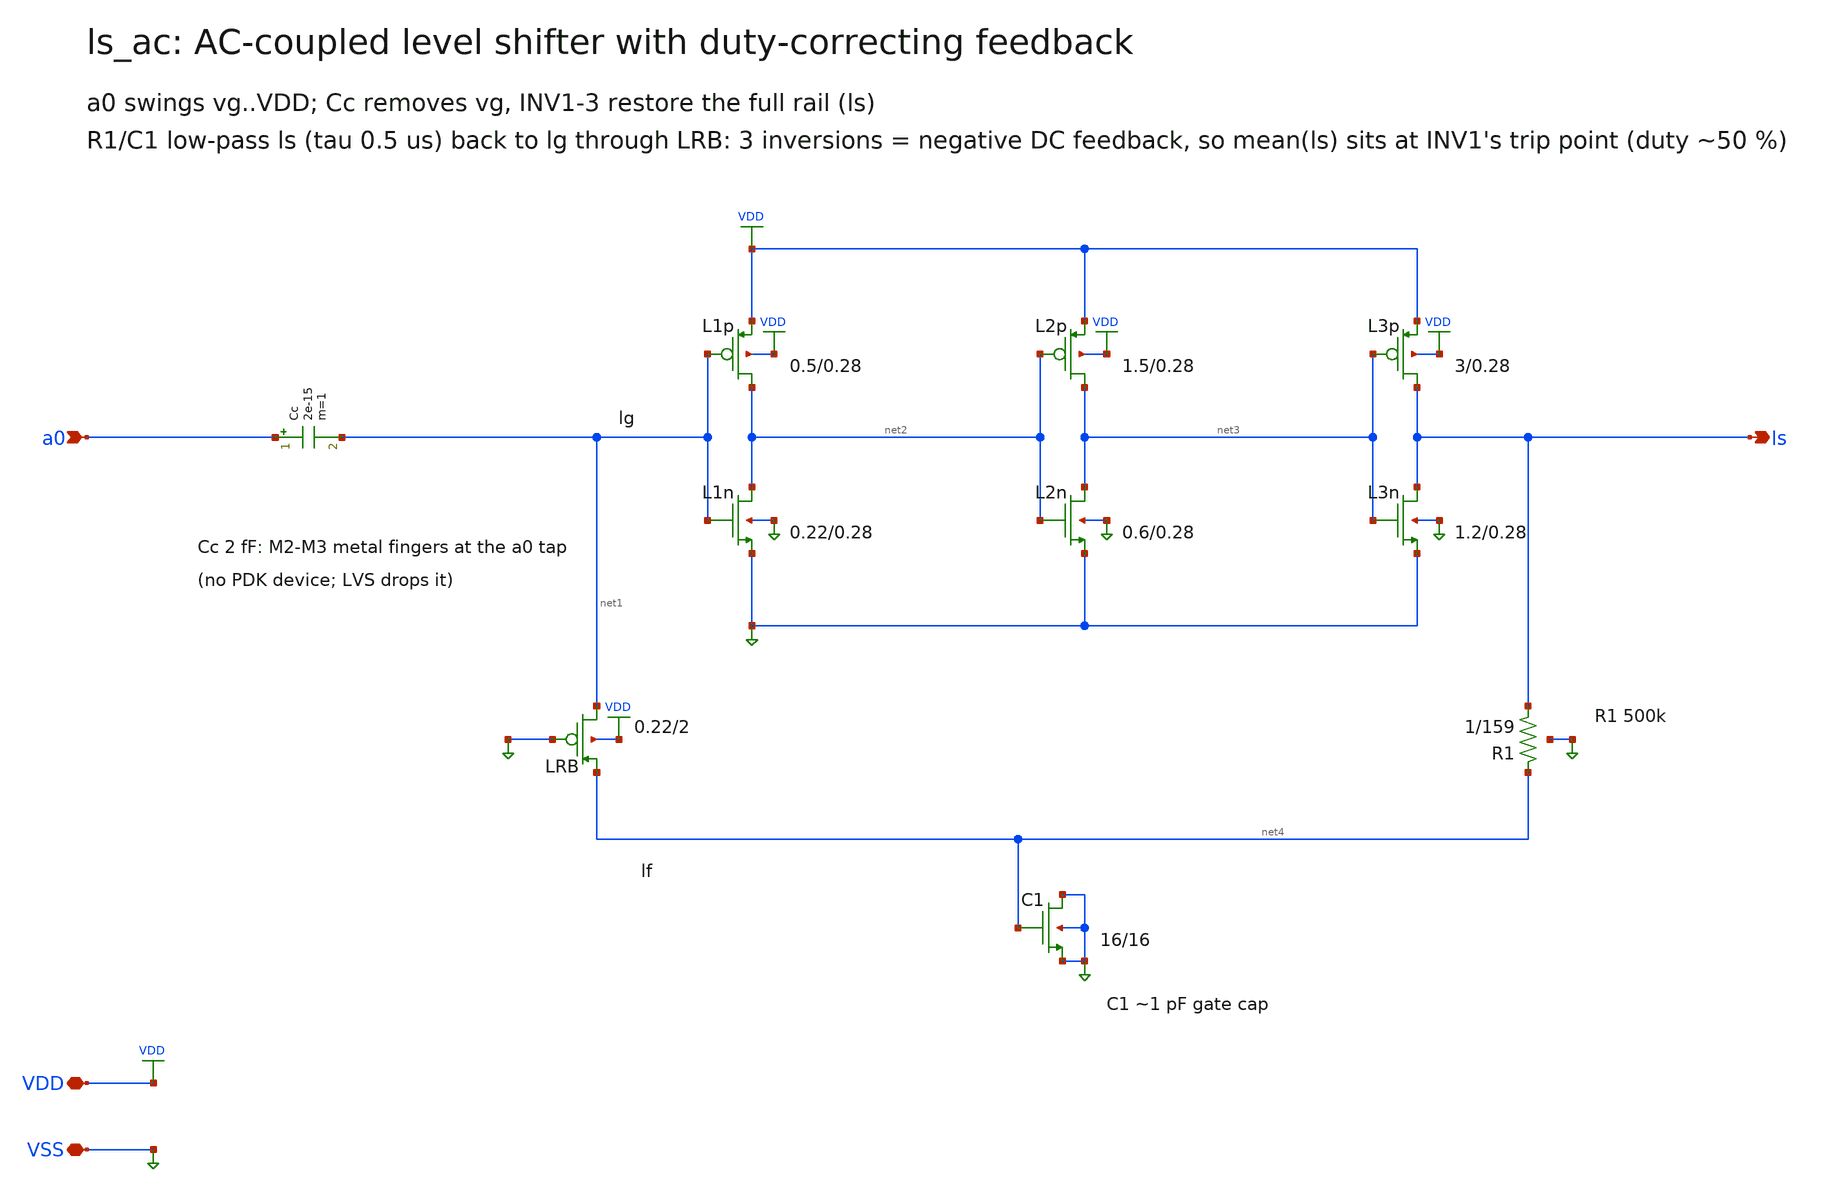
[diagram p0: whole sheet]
** sch_path: xschem/ls_ac.sch
**.subckt ls_ac VDD VSS a0 ls
*.iopin VDD
*.iopin VSS
*.ipin a0
*.opin ls
XL1p net2 net1 VDD VDD pfet_03v3 L=0.28u W=0.5u nf=1 ad=0.25p as=0.25p pd=2.0u ps=2.0u nrd=0 nrs=0
+ sa=0 sb=0 sd=0 m=1
XL1n net2 net1 VSS VSS nfet_03v3 L=0.28u W=0.21999999999999997u nf=1 ad=0.10999999999999999p
+ as=0.10999999999999999p pd=1.44u ps=1.44u nrd=0 nrs=0 sa=0 sb=0 sd=0 m=1
XL2p net3 net2 VDD VDD pfet_03v3 L=0.28u W=1.5u nf=1 ad=0.75p as=0.75p pd=4.0u ps=4.0u nrd=0 nrs=0
+ sa=0 sb=0 sd=0 m=1
XL2n net3 net2 VSS VSS nfet_03v3 L=0.28u W=0.6u nf=1 ad=0.3p as=0.3p pd=2.2u ps=2.2u nrd=0 nrs=0
+ sa=0 sb=0 sd=0 m=1
XL3p ls net3 VDD VDD pfet_03v3 L=0.28u W=3.0u nf=1 ad=1.5p as=1.5p pd=7.0u ps=7.0u nrd=0 nrs=0 sa=0
+ sb=0 sd=0 m=1
XL3n ls net3 VSS VSS nfet_03v3 L=0.28u W=1.2u nf=1 ad=0.6p as=0.6p pd=3.4u ps=3.4u nrd=0 nrs=0 sa=0
+ sb=0 sd=0 m=1
Cc a0 net1 2e-15 m=1
XLRB net1 VSS net4 VDD pfet_03v3 L=2.0u W=0.21999999999999997u nf=1 ad=0.10999999999999999p
+ as=0.10999999999999999p pd=1.44u ps=1.44u nrd=0 nrs=0 sa=0 sb=0 sd=0 m=1
XR1 ls net4 VSS ppolyf_u_3k r_width=1.0e-6 r_length=159.125e-6 m=1
XC1 VSS net4 VSS VSS nfet_03v3 L=16.0u W=16.0u nf=1 ad=8.0p as=8.0p pd=33.0u ps=33.0u nrd=0 nrs=0
+ sa=0 sb=0 sd=0 m=1
**.ends
.end
